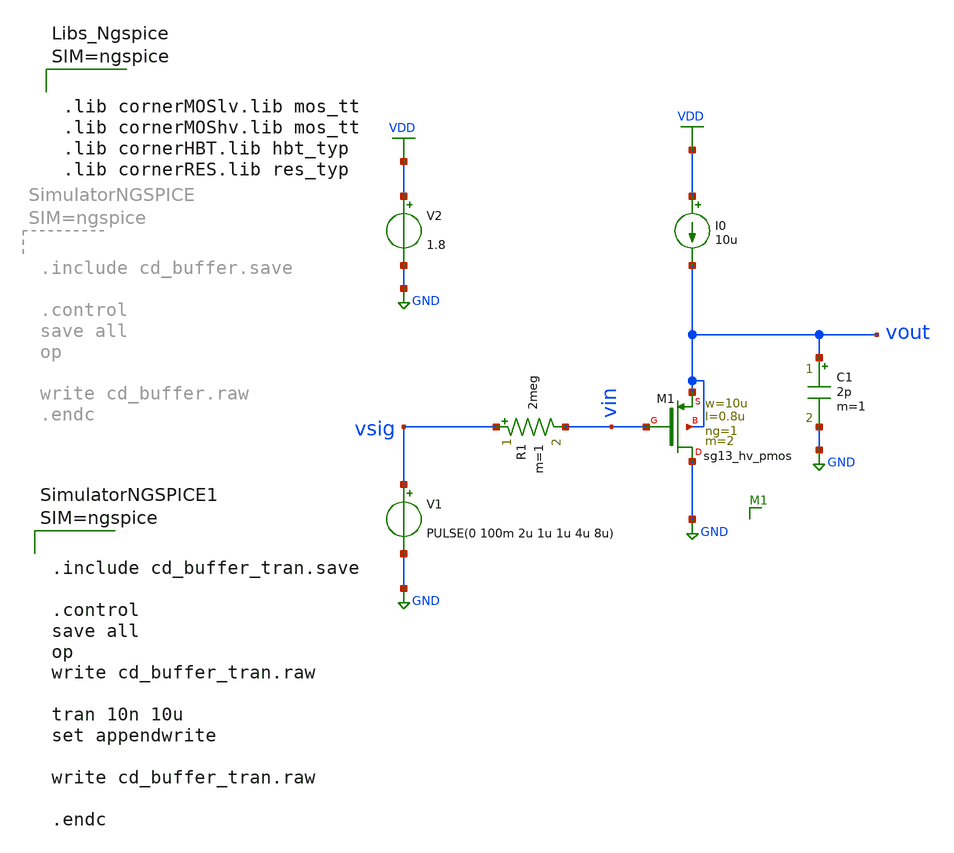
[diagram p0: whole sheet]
** sch_path: Schematics/lab_3/cd_buffer_tran.sch
**.subckt cd_buffer_tran
XM1 GND vin vout vout sg13_hv_pmos w=10u l=0.8u ng=1 m=2 mm_ok=1
R1 vsig vin 2meg m=1
V1 vsig GND PULSE(0 100m 2u 1u 1u 4u 8u)
I0 VDD vout 10u
V2 VDD GND 1.8
C1 vout GND 2p m=1
**** begin user architecture code



.lib cornerMOSlv.lib mos_tt
.lib cornerMOShv.lib mos_tt
.lib cornerHBT.lib hbt_typ
.lib cornerRES.lib res_typ






.include cd_buffer_tran.save

.control
save all
op
write cd_buffer_tran.raw

tran 10n 10u
set appendwrite

write cd_buffer_tran.raw

.endc



**** end user architecture code
**.ends
.GLOBAL GND
.GLOBAL VDD
.end
